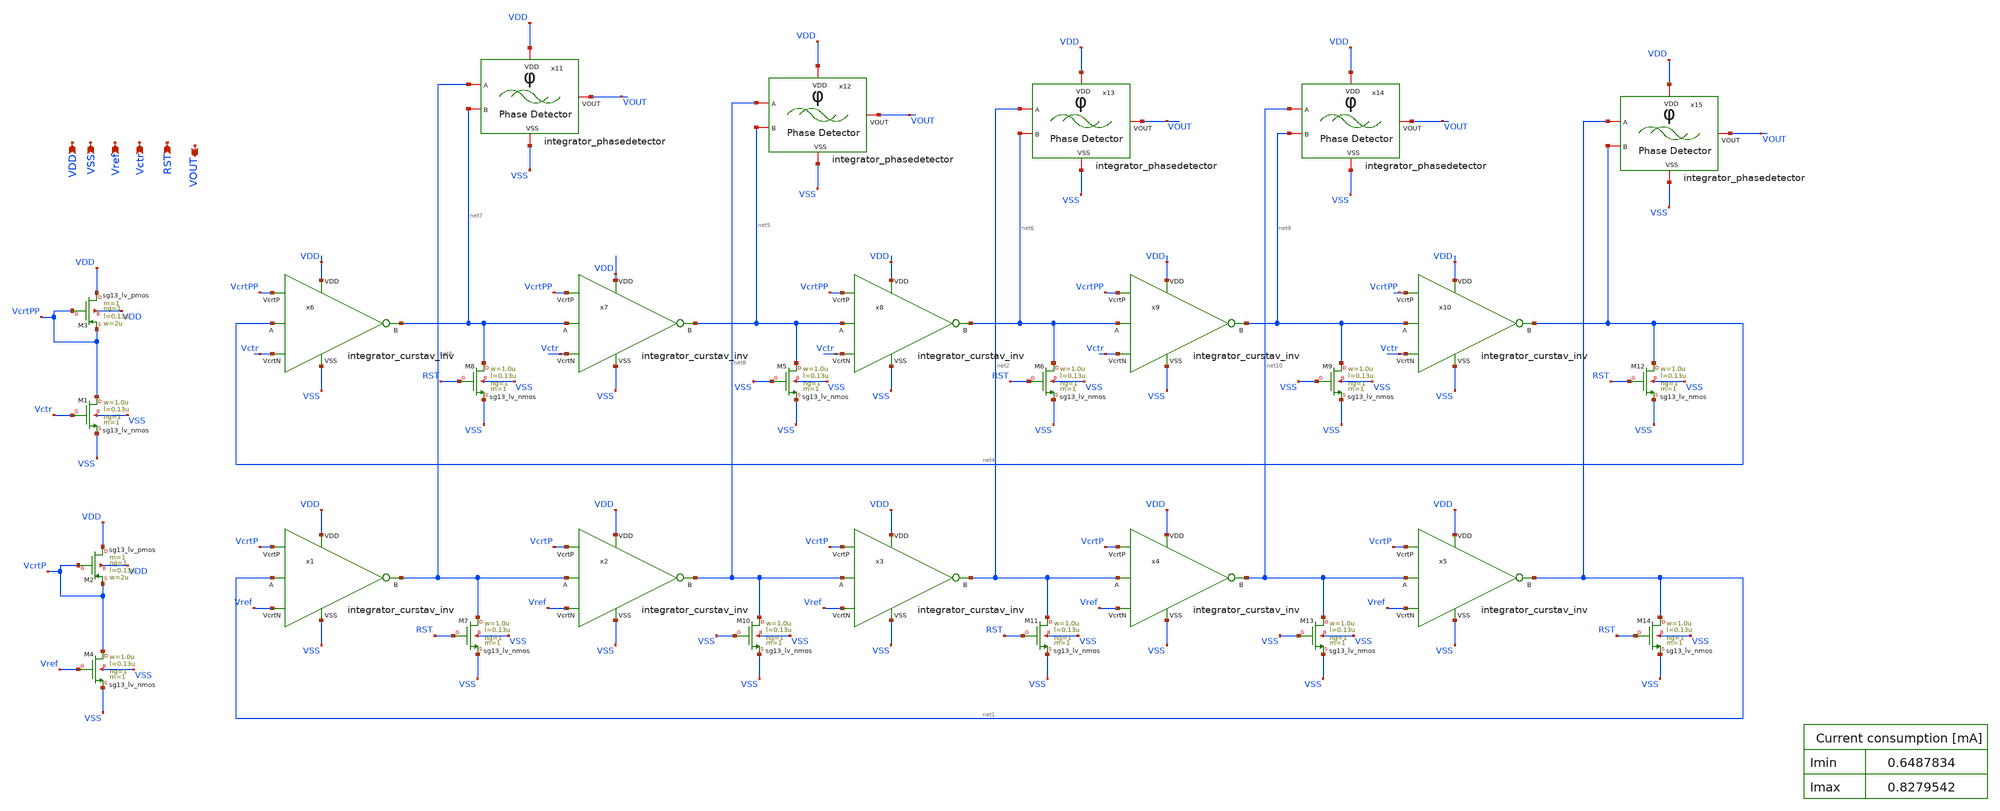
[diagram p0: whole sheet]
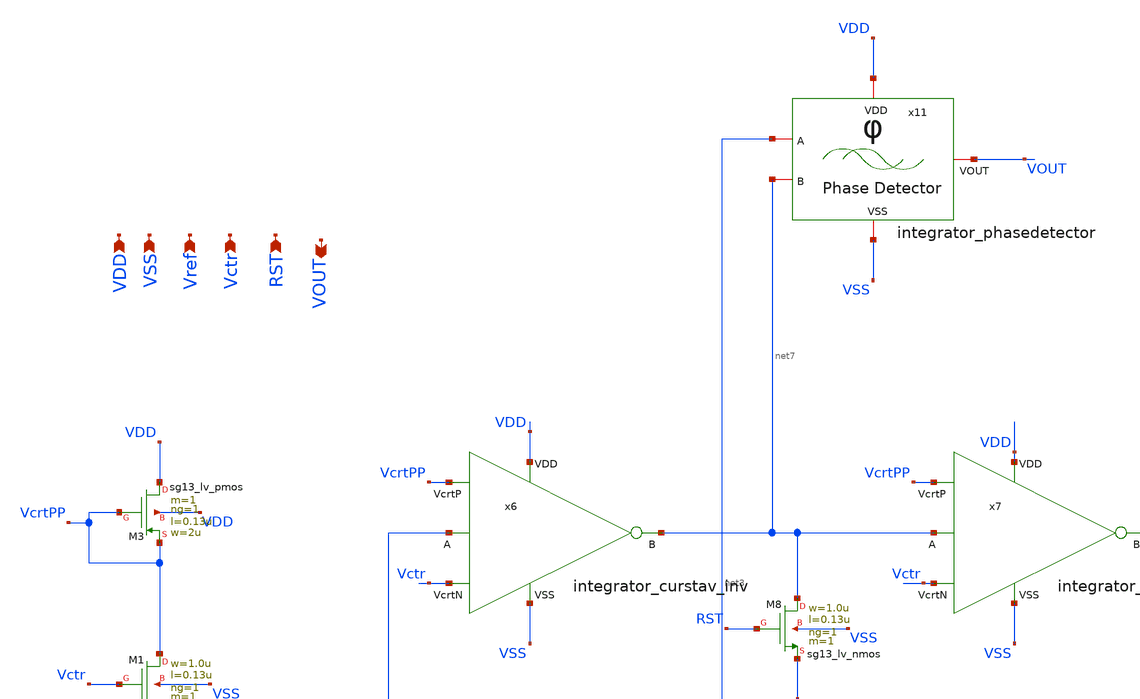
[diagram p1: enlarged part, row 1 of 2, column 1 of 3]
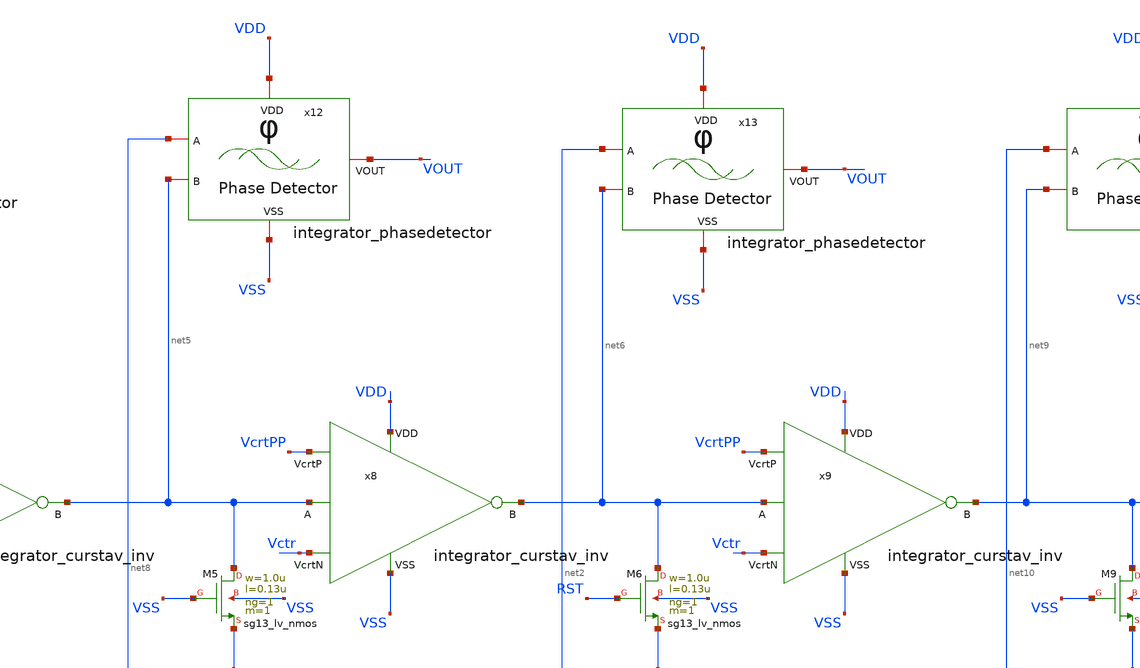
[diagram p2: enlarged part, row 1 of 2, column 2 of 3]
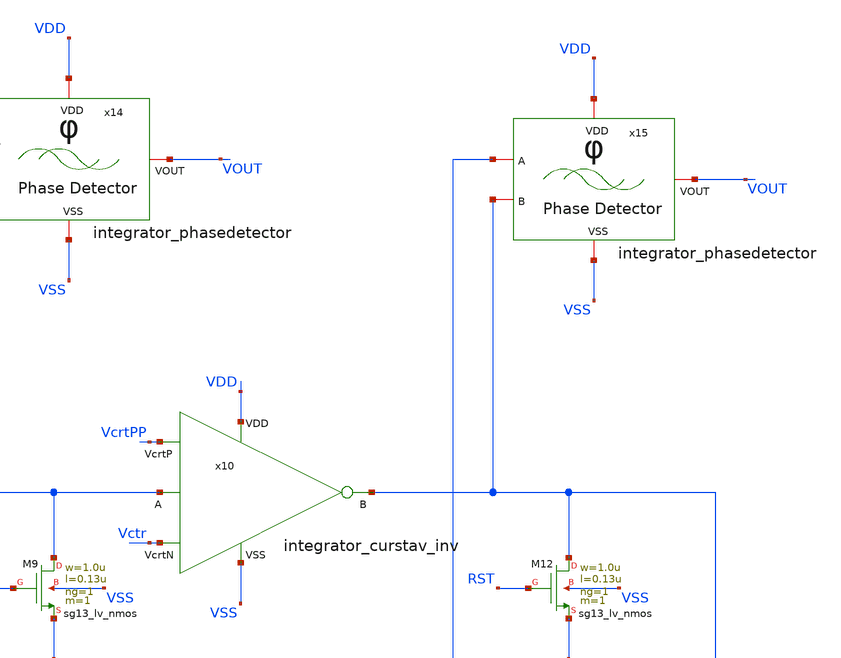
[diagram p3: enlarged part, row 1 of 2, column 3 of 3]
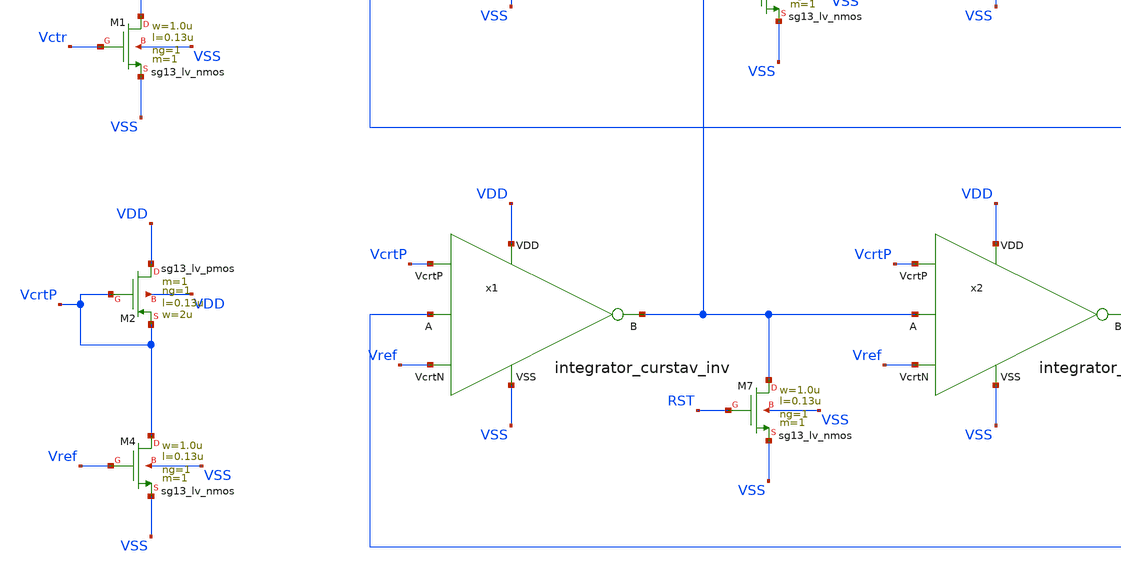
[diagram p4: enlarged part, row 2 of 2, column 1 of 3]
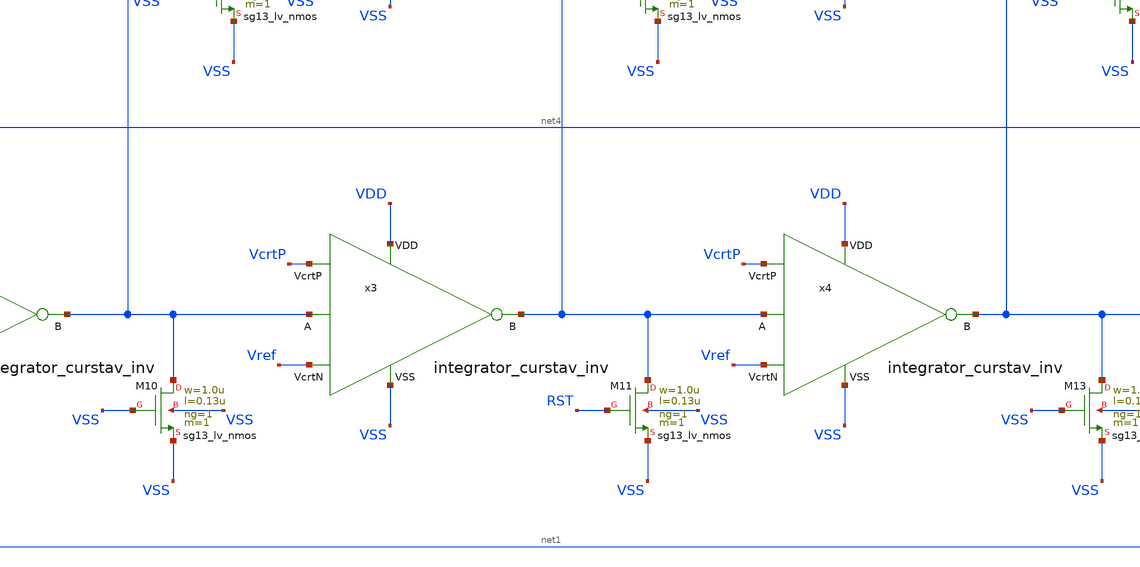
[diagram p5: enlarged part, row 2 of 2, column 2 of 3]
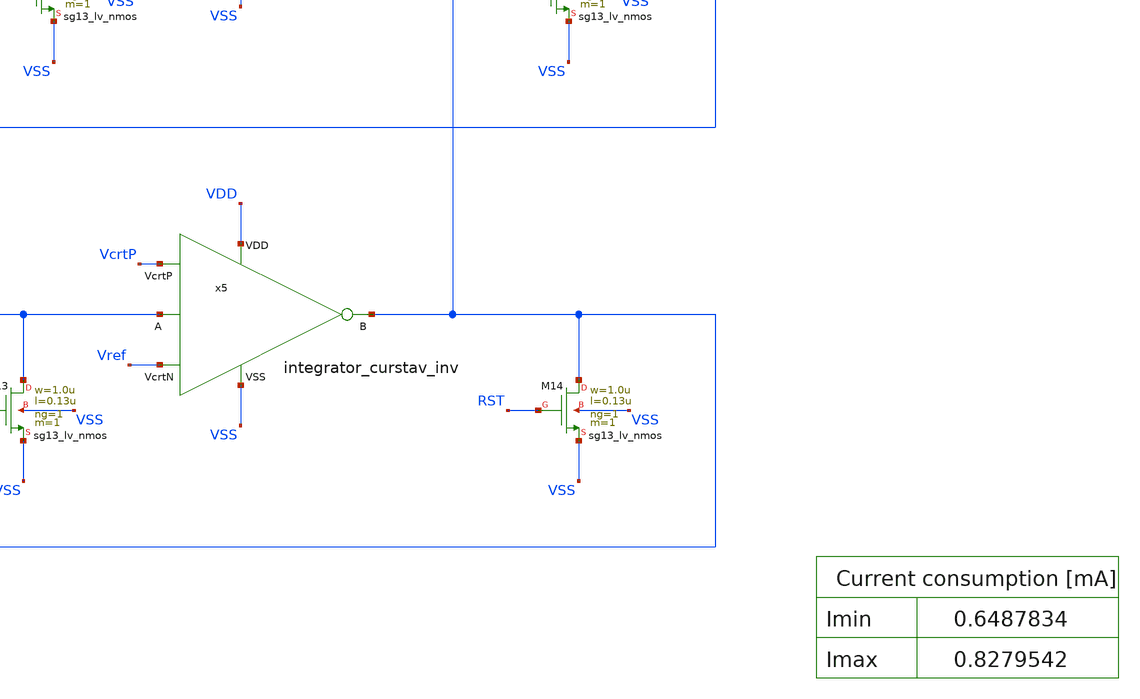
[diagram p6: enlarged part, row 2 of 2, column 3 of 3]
** sch_path: work/integrator/xschem/integrator.sch
**.subckt integrator VSS Vref Vctr VDD RST VOUT
*.ipin VSS
*.ipin Vref
*.ipin Vctr
*.ipin VDD
*.ipin RST
*.opin VOUT
x1 VDD VcrtP net1 net3 Vref VSS integrator_curstav_inv
x2 VDD VcrtP net3 net8 Vref VSS integrator_curstav_inv
x3 VDD VcrtP net8 net2 Vref VSS integrator_curstav_inv
x4 VDD VcrtP net2 net10 Vref VSS integrator_curstav_inv
x5 VDD VcrtP net10 net1 Vref VSS integrator_curstav_inv
x6 VDD VcrtPP net4 net7 Vctr VSS integrator_curstav_inv
x7 VDD VcrtPP net7 net5 Vctr VSS integrator_curstav_inv
x8 VDD VcrtPP net5 net6 Vctr VSS integrator_curstav_inv
x9 VDD VcrtPP net6 net9 Vctr VSS integrator_curstav_inv
x10 VDD VcrtPP net9 net4 Vctr VSS integrator_curstav_inv
XM8 net7 RST VSS VSS sg13_lv_nmos w=1.0u l=0.13u ng=1 m=1 mm_ok=1
x11 VDD net3 VOUT net7 VSS integrator_phasedetector
x12 VDD net8 VOUT net5 VSS integrator_phasedetector
x13 VDD net2 VOUT net6 VSS integrator_phasedetector
x14 VDD net10 VOUT net9 VSS integrator_phasedetector
x15 VDD net1 VOUT net4 VSS integrator_phasedetector
XM1 VcrtPP Vctr VSS VSS sg13_lv_nmos w=1.0u l=0.13u ng=1 m=1 mm_ok=1
XM3 VDD VcrtPP VcrtPP VDD sg13_lv_pmos w=2u l=0.13u ng=1 m=1 mm_ok=1
XM2 VDD VcrtP VcrtP VDD sg13_lv_pmos w=2u l=0.13u ng=1 m=1 mm_ok=1
XM4 VcrtP Vref VSS VSS sg13_lv_nmos w=1.0u l=0.13u ng=1 m=1 mm_ok=1
XM5 net5 VSS VSS VSS sg13_lv_nmos w=1.0u l=0.13u ng=1 m=1 mm_ok=1
XM6 net6 RST VSS VSS sg13_lv_nmos w=1.0u l=0.13u ng=1 m=1 mm_ok=1
XM9 net9 VSS VSS VSS sg13_lv_nmos w=1.0u l=0.13u ng=1 m=1 mm_ok=1
XM12 net4 RST VSS VSS sg13_lv_nmos w=1.0u l=0.13u ng=1 m=1 mm_ok=1
XM7 net3 RST VSS VSS sg13_lv_nmos w=1.0u l=0.13u ng=1 m=1 mm_ok=1
XM10 net8 VSS VSS VSS sg13_lv_nmos w=1.0u l=0.13u ng=1 m=1 mm_ok=1
XM11 net2 RST VSS VSS sg13_lv_nmos w=1.0u l=0.13u ng=1 m=1 mm_ok=1
XM13 net10 VSS VSS VSS sg13_lv_nmos w=1.0u l=0.13u ng=1 m=1 mm_ok=1
XM14 net1 RST VSS VSS sg13_lv_nmos w=1.0u l=0.13u ng=1 m=1 mm_ok=1
**.ends

* expanding   symbol:
*+  /foss/designs/chipathon_2025/designs/ihp-sg13g2/integrator_curstav_inv/xschem/integrator_curstav_inv.sym # of pins=6
** sym_path: work/integrator_curstav_inv/xschem/integrator_curstav_inv.sym
** sch_path: work/integrator_curstav_inv/xschem/integrator_curstav_inv.sch
.subckt integrator_curstav_inv VDD VcrtP A B VcrtN VSS
*.ipin VDD
*.ipin VSS
*.ipin A
*.opin B
*.ipin VcrtP
*.ipin VcrtN
XM1 B A net2 VSS sg13_lv_nmos w=1.0u l=0.13u ng=1 m=1 mm_ok=1
XM2 net2 VcrtN VSS VSS sg13_lv_nmos w=1.0u l=0.13u ng=1 m=1 mm_ok=1
XM3 net1 A B VDD sg13_lv_pmos w=2u l=0.13u ng=1 m=1 mm_ok=1
XM4 VDD VcrtP net1 VDD sg13_lv_pmos w=2u l=0.13u ng=1 m=1 mm_ok=1
.ends


* expanding   symbol:
*+  /foss/designs/chipathon_2025/designs/ihp-sg13g2/integrator_phasedetector/xschem/integrator_phasedetector.sym # of pins=5
** sym_path: /foss/designs/chipathon_2025/designs/ihp-sg13g2/integrator_phasedetector/xschem/integrator_phasedetector.sym
** sch_path: /foss/designs/chipathon_2025/designs/ihp-sg13g2/integrator_phasedetector/xschem/integrator_phasedetector.sch
.subckt integrator_phasedetector VDD A VOUT B VSS
*.ipin A
*.ipin B
*.ipin VSS
*.ipin VDD
*.opin VOUT
x1 net3 net4 net5 net6 net7 gate_xor
x2 VDD net2 net1 VSS gate_buff_L0d13
XRXOR net1 VOUT SUB rppd w=0.5e-6 l=0.5e-6 m=2 b=0 mm_ok=1
XRTAP VSS SUB ptap1 R=262.8 w=0.78e-6 l=0.78e-6
.ends


* expanding   symbol:  /foss/designs/chipathon_2025/designs/ihp-sg13g2/gate_xor/xschem/gate_xor.sym
*+ # of pins=5
** sym_path: /foss/designs/chipathon_2025/designs/ihp-sg13g2/gate_xor/xschem/gate_xor.sym
** sch_path: /foss/designs/chipathon_2025/designs/ihp-sg13g2/gate_xor/xschem/gate_xor.sch
.subckt gate_xor VDD S A B VSS
*.iopin VSS
*.iopin VDD
*.iopin S
*.iopin A
*.iopin B
XM2 S B vz VSS nfet_03v3 L=0.28u W=1u nf=1 ad='int((nf+1)/2) * W/nf * 0.18u' as='int((nf+2)/2) * W/nf * 0.18u'
+ pd='2*int((nf+1)/2) * (W/nf + 0.18u)' ps='2*int((nf+2)/2) * (W/nf + 0.18u)' nrd='0.18u / W' nrs='0.18u / W'
+ sa=0 sb=0 sd=0 m=4
XM3 S -B vx VDD pfet_03v3 L=0.28u W=3u nf=1 ad='int((nf+1)/2) * W/nf * 0.18u' as='int((nf+2)/2) * W/nf * 0.18u'
+ pd='2*int((nf+1)/2) * (W/nf + 0.18u)' ps='2*int((nf+2)/2) * (W/nf + 0.18u)' nrd='0.18u / W' nrs='0.18u / W'
+ sa=0 sb=0 sd=0 m=4
XM1 vx A VDD VDD pfet_03v3 L=0.28u W=3u nf=1 ad='int((nf+1)/2) * W/nf * 0.18u' as='int((nf+2)/2) * W/nf * 0.18u'
+ pd='2*int((nf+1)/2) * (W/nf + 0.18u)' ps='2*int((nf+2)/2) * (W/nf + 0.18u)' nrd='0.18u / W' nrs='0.18u / W'
+ sa=0 sb=0 sd=0 m=4
XM4 S -B vw VSS nfet_03v3 L=0.28u W=1u nf=1 ad='int((nf+1)/2) * W/nf * 0.18u' as='int((nf+2)/2) * W/nf * 0.18u'
+ pd='2*int((nf+1)/2) * (W/nf + 0.18u)' ps='2*int((nf+2)/2) * (W/nf + 0.18u)' nrd='0.18u / W' nrs='0.18u / W'
+ sa=0 sb=0 sd=0 m=4
XM5 S B vy VDD pfet_03v3 L=0.28u W=3u nf=1 ad='int((nf+1)/2) * W/nf * 0.18u' as='int((nf+2)/2) * W/nf * 0.18u'
+ pd='2*int((nf+1)/2) * (W/nf + 0.18u)' ps='2*int((nf+2)/2) * (W/nf + 0.18u)' nrd='0.18u / W' nrs='0.18u / W'
+ sa=0 sb=0 sd=0 m=4
XM6 vy -A VDD VDD pfet_03v3 L=0.28u W=3u nf=1 ad='int((nf+1)/2) * W/nf * 0.18u' as='int((nf+2)/2) * W/nf * 0.18u'
+ pd='2*int((nf+1)/2) * (W/nf + 0.18u)' ps='2*int((nf+2)/2) * (W/nf + 0.18u)' nrd='0.18u / W' nrs='0.18u / W'
+ sa=0 sb=0 sd=0 m=4
XM7 vz A VSS VSS nfet_03v3 L=0.28u W=1u nf=1 ad='int((nf+1)/2) * W/nf * 0.18u' as='int((nf+2)/2) * W/nf * 0.18u'
+ pd='2*int((nf+1)/2) * (W/nf + 0.18u)' ps='2*int((nf+2)/2) * (W/nf + 0.18u)' nrd='0.18u / W' nrs='0.18u / W'
+ sa=0 sb=0 sd=0 m=4
XM8 vw -A VSS VSS nfet_03v3 L=0.28u W=1u nf=1 ad='int((nf+1)/2) * W/nf * 0.18u' as='int((nf+2)/2) * W/nf * 0.18u'
+ pd='2*int((nf+1)/2) * (W/nf + 0.18u)' ps='2*int((nf+2)/2) * (W/nf + 0.18u)' nrd='0.18u / W' nrs='0.18u / W'
+ sa=0 sb=0 sd=0 m=4
xINVA VDD -A A VSS gate_inv_L0d28
xINVB VDD -B B VSS gate_inv_L0d28
XM10 VDD VDD vx VDD pfet_03v3 L=0.28u W=3u nf=1 ad='int((nf+1)/2) * W/nf * 0.18u' as='int((nf+2)/2) * W/nf * 0.18u'
+ pd='2*int((nf+1)/2) * (W/nf + 0.18u)' ps='2*int((nf+2)/2) * (W/nf + 0.18u)' nrd='0.18u / W' nrs='0.18u / W'
+ sa=0 sb=0 sd=0 m=2
XM11 VDD VDD vy VDD pfet_03v3 L=0.28u W=3u nf=1 ad='int((nf+1)/2) * W/nf * 0.18u' as='int((nf+2)/2) * W/nf * 0.18u'
+ pd='2*int((nf+1)/2) * (W/nf + 0.18u)' ps='2*int((nf+2)/2) * (W/nf + 0.18u)' nrd='0.18u / W' nrs='0.18u / W'
+ sa=0 sb=0 sd=0 m=2
XM13 vz VSS VSS VSS nfet_03v3 L=0.28u W=1u nf=1 ad='int((nf+1)/2) * W/nf * 0.18u' as='int((nf+2)/2) * W/nf * 0.18u'
+ pd='2*int((nf+1)/2) * (W/nf + 0.18u)' ps='2*int((nf+2)/2) * (W/nf + 0.18u)' nrd='0.18u / W' nrs='0.18u / W'
+ sa=0 sb=0 sd=0 m=2
XM14 vw VSS VSS VSS nfet_03v3 L=0.28u W=1u nf=1 ad='int((nf+1)/2) * W/nf * 0.18u' as='int((nf+2)/2) * W/nf * 0.18u'
+ pd='2*int((nf+1)/2) * (W/nf + 0.18u)' ps='2*int((nf+2)/2) * (W/nf + 0.18u)' nrd='0.18u / W' nrs='0.18u / W'
+ sa=0 sb=0 sd=0 m=2
.ends


* expanding   symbol:
*+  /foss/designs/chipathon_2025/designs/ihp-sg13g2/gate_buff_L0d13/xschem/gate_buff_L0d13.sym # of pins=4
** sym_path: /foss/designs/chipathon_2025/designs/ihp-sg13g2/gate_buff_L0d13/xschem/gate_buff_L0d13.sym
** sch_path: /foss/designs/chipathon_2025/designs/ihp-sg13g2/gate_buff_L0d13/xschem/gate_buff_L0d13.sch
.subckt gate_buff_L0d13 VDD VIN VOUT VSS
*.ipin VDD
*.ipin VIN
*.ipin VSS
*.opin VOUT
XM1 net1 VIN VSS VSS sg13_lv_nmos w=1.0u l=0.13u ng=1 m=1 mm_ok=1
XM2 VDD VIN net1 VDD sg13_lv_pmos w=2u l=0.13u ng=1 m=1 mm_ok=1
XM3 VOUT net1 VSS VSS sg13_lv_nmos w=1.0u l=0.13u ng=1 m=3 mm_ok=1
XM4 VDD net1 VOUT VDD sg13_lv_pmos w=2u l=0.13u ng=1 m=3 mm_ok=1
.ends


* expanding   symbol:
*+  /foss/designs/chipathon_2025/designs/gf180/gate_inv_L0d28/xschem/gate_inv_L0d28.sym # of pins=4
** sym_path: /foss/designs/chipathon_2025/designs/gf180/gate_inv_L0d28/xschem/gate_inv_L0d28.sym
** sch_path: /foss/designs/chipathon_2025/designs/gf180/gate_inv_L0d28/xschem/gate_inv_L0d28.sch
.subckt gate_inv_L0d28 VDD B A VSS
*.opin B
*.ipin A
*.iopin VDD
*.iopin VSS
XMN B A VSS VSS nfet_03v3 L=0.28u W=1u nf=1 ad='int((nf+1)/2) * W/nf * 0.18u' as='int((nf+2)/2) * W/nf * 0.18u'
+ pd='2*int((nf+1)/2) * (W/nf + 0.18u)' ps='2*int((nf+2)/2) * (W/nf + 0.18u)' nrd='0.18u / W' nrs='0.18u / W'
+ sa=0 sb=0 sd=0 m=2
XMP B A VDD VDD pfet_03v3 L=0.28u W=3u nf=1 ad='int((nf+1)/2) * W/nf * 0.18u' as='int((nf+2)/2) * W/nf * 0.18u'
+ pd='2*int((nf+1)/2) * (W/nf + 0.18u)' ps='2*int((nf+2)/2) * (W/nf + 0.18u)' nrd='0.18u / W' nrs='0.18u / W'
+ sa=0 sb=0 sd=0 m=2
.ends

.GLOBAL SUB
.end
